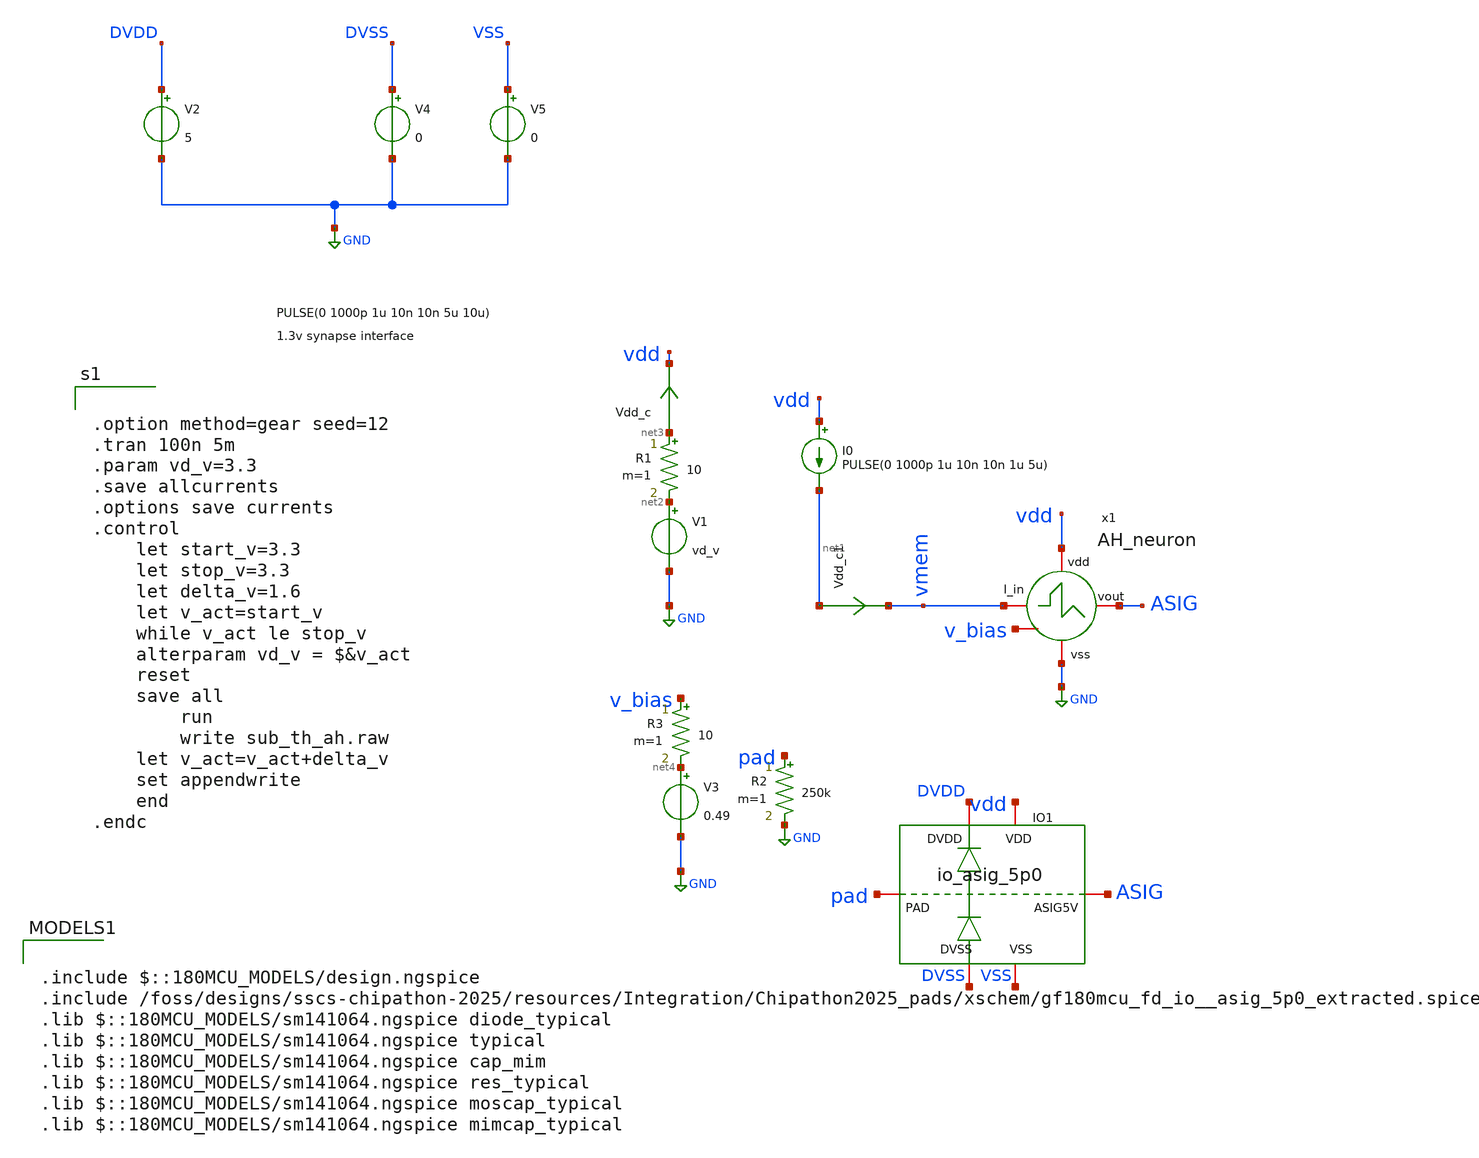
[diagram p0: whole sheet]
** sch_path: designs/libs/tb_core_analogs_pads/tb_AH_neuron/AH_neuron.sch
**.subckt AH_neuron
V1 net2 GND vd_v
Vdd_c net3 vdd 0
.save i(vdd_c)
I0 vdd net1 PULSE(0 1000p 1u 10n 10n 1u 5u)
x1 vdd vmem ASIG GND v_bias AH_neuron
R1 net3 net2 10 m=1
R2 pad GND 250k m=1
Vdd_c1 net1 vmem 0
.save i(vdd_c1)
V2 DVDD GND 5
V4 DVSS GND 0
V5 VSS GND 0
XIO1 DVSS DVDD VSS vdd pad ASIG gf180mcu_fd_io__asig_5p0_extracted
V3 net4 GND 0.49
R3 v_bias net4 10 m=1
**** begin user architecture code


.option method=gear seed=12
.tran 100n 5m
.param vd_v=3.3
.save allcurrents
.options save currents
.control
    let start_v=3.3
    let stop_v=3.3
    let delta_v=1.6
    let v_act=start_v
    while v_act le stop_v
	alterparam vd_v = $&v_act
	reset
	save all
        run
        write sub_th_ah.raw
	let v_act=v_act+delta_v
	set appendwrite
    end
.endc



.include $::180MCU_MODELS/design.ngspice
.include /foss/designs/sscs-chipathon-2025/resources/Integration/Chipathon2025_pads/xschem/gf180mcu_fd_io__asig_5p0_extracted.spice
.lib $::180MCU_MODELS/sm141064.ngspice diode_typical
.lib $::180MCU_MODELS/sm141064.ngspice typical
.lib $::180MCU_MODELS/sm141064.ngspice cap_mim
.lib $::180MCU_MODELS/sm141064.ngspice res_typical
.lib $::180MCU_MODELS/sm141064.ngspice moscap_typical
.lib $::180MCU_MODELS/sm141064.ngspice mimcap_typical

**** end user architecture code
**.ends
.GLOBAL GND
.end
